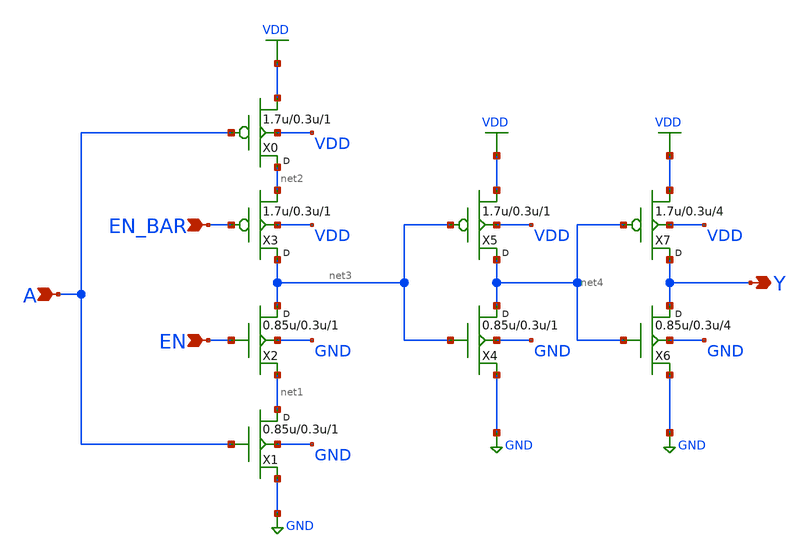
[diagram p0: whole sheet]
** sch_path: gf180mcu_osu_sc_gp9t3v3/cells/tinv/gf180mcu_osu_sc_gp9t3v3__tinv_4.sch
**.subckt gf180mcu_osu_sc_gp9t3v3__tinv_4 A Y EN_BAR EN
*.ipin A
*.opin Y
*.ipin EN_BAR
*.ipin EN
X0 net2 A VDD VDD pmos_3p3 w=1.7u l=0.3u m=1
X1 net1 A GND GND nmos_3p3 w=0.85u l=0.3u m=1
X2 net3 EN net1 GND nmos_3p3 w=0.85u l=0.3u m=1
X3 net3 EN_BAR net2 VDD pmos_3p3 w=1.7u l=0.3u m=1
X4 net4 net3 GND GND nmos_3p3 w=0.85u l=0.3u m=1
X5 net4 net3 VDD VDD pmos_3p3 w=1.7u l=0.3u m=1
X6 Y net4 GND GND nmos_3p3 w=0.85u l=0.3u m=4
X7 Y net4 VDD VDD pmos_3p3 w=1.7u l=0.3u m=4
**.ends
.GLOBAL VDD
.GLOBAL GND
.end
